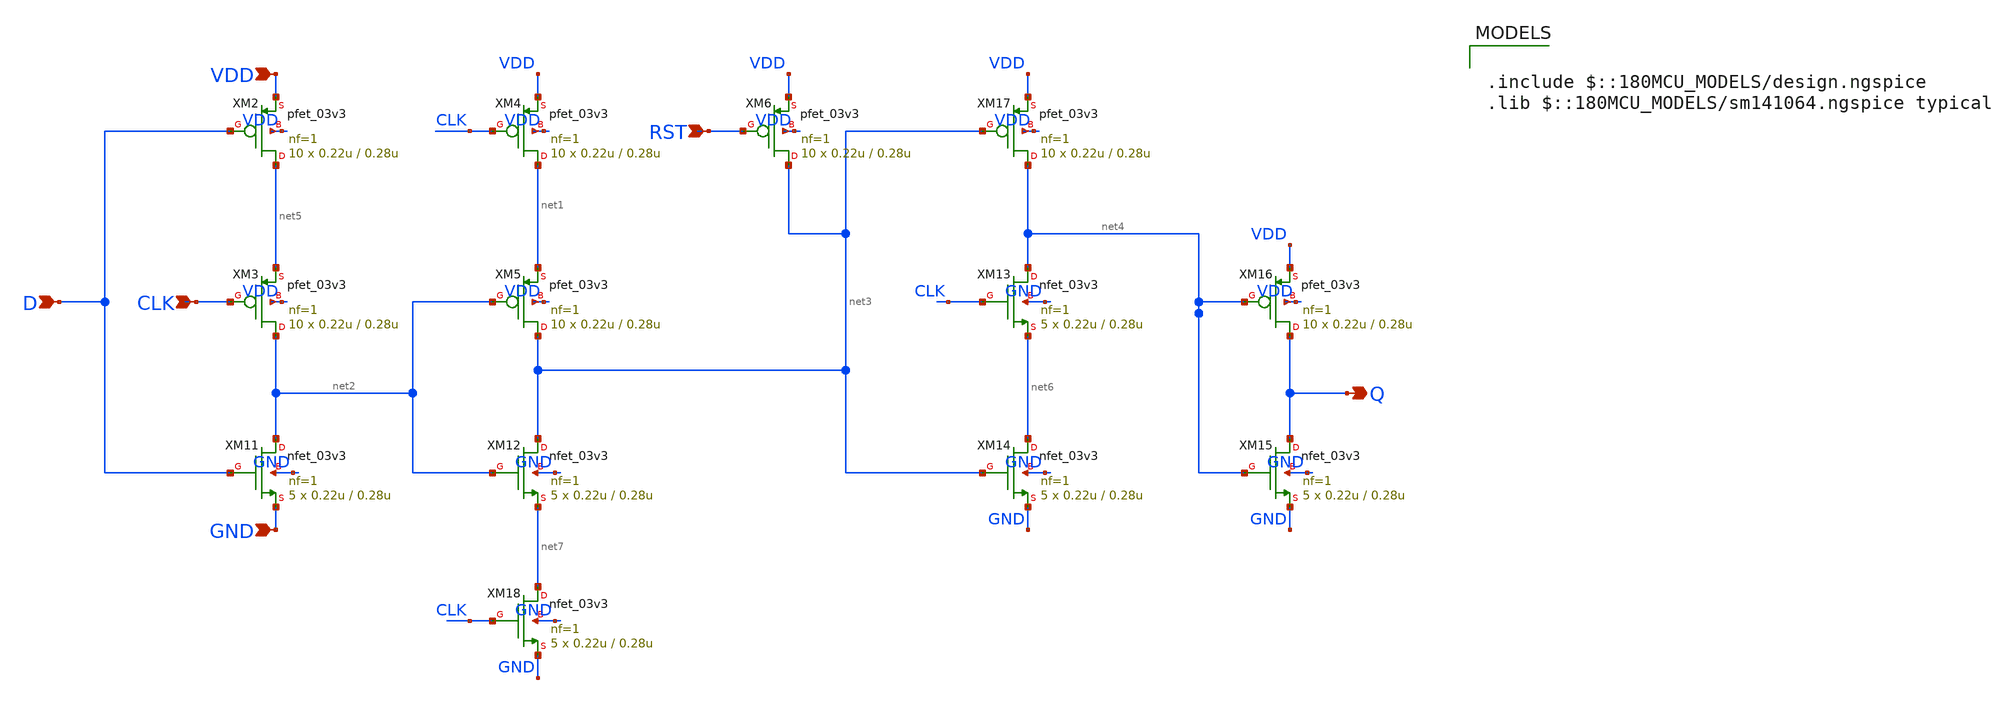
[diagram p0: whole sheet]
** sch_path: blocks/adc/encoder/tb/dff_test.sch
**.subckt dff_test Q D CLK RST VDD GND
*.opin Q
*.ipin D
*.ipin CLK
*.ipin RST
*.ipin VDD
*.ipin GND
XM2 net5 D VDD VDD pfet_03v3 L=0.28u W=0.22u nf=1 ad='int((nf+1)/2) * W/nf * 0.18u' as='int((nf+2)/2) * W/nf * 0.18u'
+ pd='2*int((nf+1)/2) * (W/nf + 0.18u)' ps='2*int((nf+2)/2) * (W/nf + 0.18u)' nrd='0.18u / W' nrs='0.18u / W'
+ sa=0 sb=0 sd=0 m=10
XM3 net2 CLK net5 VDD pfet_03v3 L=0.28u W=0.22u nf=1 ad='int((nf+1)/2) * W/nf * 0.18u' as='int((nf+2)/2) * W/nf * 0.18u'
+ pd='2*int((nf+1)/2) * (W/nf + 0.18u)' ps='2*int((nf+2)/2) * (W/nf + 0.18u)' nrd='0.18u / W' nrs='0.18u / W'
+ sa=0 sb=0 sd=0 m=10
XM4 net1 CLK VDD VDD pfet_03v3 L=0.28u W=0.22u nf=1 ad='int((nf+1)/2) * W/nf * 0.18u' as='int((nf+2)/2) * W/nf * 0.18u'
+ pd='2*int((nf+1)/2) * (W/nf + 0.18u)' ps='2*int((nf+2)/2) * (W/nf + 0.18u)' nrd='0.18u / W' nrs='0.18u / W'
+ sa=0 sb=0 sd=0 m=10
XM5 net3 net2 net1 VDD pfet_03v3 L=0.28u W=0.22u nf=1 ad='int((nf+1)/2) * W/nf * 0.18u' as='int((nf+2)/2) * W/nf * 0.18u'
+ pd='2*int((nf+1)/2) * (W/nf + 0.18u)' ps='2*int((nf+2)/2) * (W/nf + 0.18u)' nrd='0.18u / W' nrs='0.18u / W'
+ sa=0 sb=0 sd=0 m=10
XM6 net3 RST VDD VDD pfet_03v3 L=0.28u W=0.22u nf=1 ad='int((nf+1)/2) * W/nf * 0.18u' as='int((nf+2)/2) * W/nf * 0.18u'
+ pd='2*int((nf+1)/2) * (W/nf + 0.18u)' ps='2*int((nf+2)/2) * (W/nf + 0.18u)' nrd='0.18u / W' nrs='0.18u / W'
+ sa=0 sb=0 sd=0 m=10
XM11 net2 D GND GND nfet_03v3 L=0.28u W=0.22u nf=1 ad='int((nf+1)/2) * W/nf * 0.18u' as='int((nf+2)/2) * W/nf * 0.18u'
+ pd='2*int((nf+1)/2) * (W/nf + 0.18u)' ps='2*int((nf+2)/2) * (W/nf + 0.18u)' nrd='0.18u / W' nrs='0.18u / W'
+ sa=0 sb=0 sd=0 m=5
XM12 net3 net2 net7 GND nfet_03v3 L=0.28u W=0.22u nf=1 ad='int((nf+1)/2) * W/nf * 0.18u' as='int((nf+2)/2) * W/nf * 0.18u'
+ pd='2*int((nf+1)/2) * (W/nf + 0.18u)' ps='2*int((nf+2)/2) * (W/nf + 0.18u)' nrd='0.18u / W' nrs='0.18u / W'
+ sa=0 sb=0 sd=0 m=5
XM13 net4 CLK net6 GND nfet_03v3 L=0.28u W=0.22u nf=1 ad='int((nf+1)/2) * W/nf * 0.18u' as='int((nf+2)/2) * W/nf * 0.18u'
+ pd='2*int((nf+1)/2) * (W/nf + 0.18u)' ps='2*int((nf+2)/2) * (W/nf + 0.18u)' nrd='0.18u / W' nrs='0.18u / W'
+ sa=0 sb=0 sd=0 m=5
XM14 net6 net3 GND GND nfet_03v3 L=0.28u W=0.22u nf=1 ad='int((nf+1)/2) * W/nf * 0.18u' as='int((nf+2)/2) * W/nf * 0.18u'
+ pd='2*int((nf+1)/2) * (W/nf + 0.18u)' ps='2*int((nf+2)/2) * (W/nf + 0.18u)' nrd='0.18u / W' nrs='0.18u / W'
+ sa=0 sb=0 sd=0 m=5
XM15 Q net4 GND GND nfet_03v3 L=0.28u W=0.22u nf=1 ad='int((nf+1)/2) * W/nf * 0.18u' as='int((nf+2)/2) * W/nf * 0.18u'
+ pd='2*int((nf+1)/2) * (W/nf + 0.18u)' ps='2*int((nf+2)/2) * (W/nf + 0.18u)' nrd='0.18u / W' nrs='0.18u / W'
+ sa=0 sb=0 sd=0 m=5
XM16 Q net4 VDD VDD pfet_03v3 L=0.28u W=0.22u nf=1 ad='int((nf+1)/2) * W/nf * 0.18u' as='int((nf+2)/2) * W/nf * 0.18u'
+ pd='2*int((nf+1)/2) * (W/nf + 0.18u)' ps='2*int((nf+2)/2) * (W/nf + 0.18u)' nrd='0.18u / W' nrs='0.18u / W'
+ sa=0 sb=0 sd=0 m=10
XM17 net4 net3 VDD VDD pfet_03v3 L=0.28u W=0.22u nf=1 ad='int((nf+1)/2) * W/nf * 0.18u' as='int((nf+2)/2) * W/nf * 0.18u'
+ pd='2*int((nf+1)/2) * (W/nf + 0.18u)' ps='2*int((nf+2)/2) * (W/nf + 0.18u)' nrd='0.18u / W' nrs='0.18u / W'
+ sa=0 sb=0 sd=0 m=10
XM18 net7 CLK GND GND nfet_03v3 L=0.28u W=0.22u nf=1 ad='int((nf+1)/2) * W/nf * 0.18u' as='int((nf+2)/2) * W/nf * 0.18u'
+ pd='2*int((nf+1)/2) * (W/nf + 0.18u)' ps='2*int((nf+2)/2) * (W/nf + 0.18u)' nrd='0.18u / W' nrs='0.18u / W'
+ sa=0 sb=0 sd=0 m=5
**** begin user architecture code

.include $::180MCU_MODELS/design.ngspice
.lib $::180MCU_MODELS/sm141064.ngspice typical



V_VDD VDD 0 3.3

V_CLK CLK 0 pulse(0 3.3 0s 10p 10p 240p 500p)
V_D D 0 pwl(0 0 250p 0 260p 3.3 1.25n 3.3 1.26n 0 1.75n 0 1.76n 3.3 2.25n 3.3 2.26n 0 3.25n 0 3.26n
+ 3.3 3.75n 3.3 3.76n 0 4.25n 0 4.26n 3.3 6n 3.3)
V_RST RST 0 pulse(3.3 3.3 0s 10p 10p 240p 500p)
.control
  save CLK D RST Q
  run
  write tspc_dff_rst_test.raw
.endc
.tran 1p 5n



**** end user architecture code
**.ends
.end
